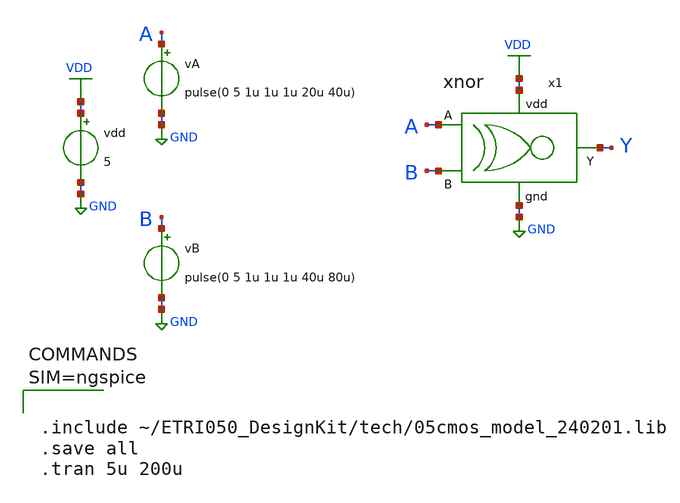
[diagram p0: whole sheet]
** sch_path: lab7/sch/tb_xnor.sch
**.subckt tb_xnor
x1 VDD GND A B Y XNOR
vA A GND pulse(0 5 1u 1u 1u 20u 40u)
vB B GND pulse(0 5 1u 1u 1u 40u 80u)
vdd VDD GND 5
**** begin user architecture code



.include ~/ETRI050_DesignKit/tech/05cmos_model_240201.lib
.save all
.tran 5u 200u



**** end user architecture code
**.ends

* expanding   symbol:  /home/dayesong/ETRI050_DesignKit/lab7/sch/XNOR.sym # of pins=6
** sym_path: lab7/sch/XNOR.sym
** sch_path: lab7/sch/XNOR.sch
.subckt XNOR vdd gnd A B Y
*.ipin A
*.ipin B
*.opin Y
*.iopin vdd
*.iopin gnd
x1 A B net3 vdd gnd nand
x2 net3 net4 net1 vdd gnd nand
x4 A B net2 vdd gnd nor
x5 net1 net5 vdd gnd inv
x3 net2 net4 vdd gnd inv
x6 net5 Y vdd gnd inv
.ends


* expanding   symbol:  /home/dayesong/ETRI050_DesignKit/lab7/sch/nand.sym # of pins=5
** sym_path: lab7/sch/nand.sym
** sch_path: lab7/sch/nand.sch
.subckt nand A B Y vdd gnd
*.ipin A
*.ipin B
*.opin Y
*.iopin vdd
*.iopin gnd
M3 net1 A gnd gnd nfet w=6u l=0.6u m=1
M4 Y B vdd vdd pfet w=6u l=0.6u m=1
M2 Y A vdd vdd pfet w=6u l=0.6u m=1
M1 Y B net1 gnd nfet w=6u l=0.6u m=1
.ends


* expanding   symbol:  /home/dayesong/ETRI050_DesignKit/lab7/sch/nor.sym # of pins=5
** sym_path: lab7/sch/nor.sym
** sch_path: lab7/sch/nor.sch
.subckt nor A B Y vdd gnd
*.ipin A
*.ipin B
*.opin Y
*.iopin vdd
*.iopin gnd
M3 net1 A vdd vdd pfet w=12u l=0.6u m=1
M4 Y A gnd gnd nfet w=3u l=0.6u m=1
M1 Y B gnd gnd nfet w=3u l=0.6u m=1
M2 Y B net1 vdd pfet w=12u l=0.6u m=1
.ends


* expanding   symbol:  /home/dayesong/ETRI050_DesignKit/lab7/sch/inv.sym # of pins=4
** sym_path: lab7/sch/inv.sym
** sch_path: lab7/sch/inv.sch
.subckt inv A Y vdd gnd
*.ipin A
*.opin Y
*.iopin vdd
*.iopin gnd
M1 Y A vdd vdd pfet w=6u l=0.6u m=1
M2 Y A gnd gnd nfet w=3u l=0.6u m=1
.ends

.GLOBAL VDD
.GLOBAL GND
.end
